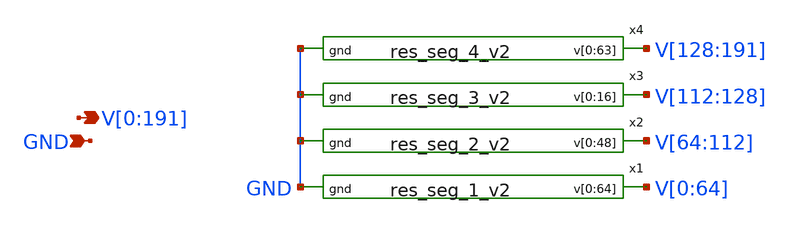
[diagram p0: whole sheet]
** sch_path: xschem/rstring_v2.sch
**.subckt rstring_v2
*+ V[0],V[1],V[2],V[3],V[4],V[5],V[6],V[7],V[8],V[9],V[10],V[11],V[12],V[13],V[14],V[15],V[16],V[17],V[18],V[19],V[20],V[21],V[22],V[23],V[24],V[25],V[26],V[27],V[28],V[29],V[30],V[31],V[32],V[33],V[34],V[35],V[36],V[37],V[38],V[39],V[40],V[41],V[42],V[43],V[44],V[45],V[46],V[47],V[48],V[49],V[50],V[51],V[52],V[53],V[54],V[55],V[56],V[57],V[58],V[59],V[60],V[61],V[62],V[63],V[64],V[65],V[66],V[67],V[68],V[69],V[70],V[71],V[72],V[73],V[74],V[75],V[76],V[77],V[78],V[79],V[80],V[81],V[82],V[83],V[84],V[85],V[86],V[87],V[88],V[89],V[90],V[91],V[92],V[93],V[94],V[95],V[96],V[97],V[98],V[99],V[100],V[101],V[102],V[103],V[104],V[105],V[106],V[107],V[108],V[109],V[110],V[111],V[112],V[113],V[114],V[115],V[116],V[117],V[118],V[119],V[120],V[121],V[122],V[123],V[124],V[125],V[126],V[127],V[128],V[129],V[130],V[131],V[132],V[133],V[134],V[135],V[136],V[137],V[138],V[139],V[140],V[141],V[142],V[143],V[144],V[145],V[146],V[147],V[148],V[149],V[150],V[151],V[152],V[153],V[154],V[155],V[156],V[157],V[158],V[159],V[160],V[161],V[162],V[163],V[164],V[165],V[166],V[167],V[168],V[169],V[170],V[171],V[172],V[173],V[174],V[175],V[176],V[177],V[178],V[179],V[180],V[181],V[182],V[183],V[184],V[185],V[186],V[187],V[188],V[189],V[190],V[191] GND
*.opin
*+ V[0],V[1],V[2],V[3],V[4],V[5],V[6],V[7],V[8],V[9],V[10],V[11],V[12],V[13],V[14],V[15],V[16],V[17],V[18],V[19],V[20],V[21],V[22],V[23],V[24],V[25],V[26],V[27],V[28],V[29],V[30],V[31],V[32],V[33],V[34],V[35],V[36],V[37],V[38],V[39],V[40],V[41],V[42],V[43],V[44],V[45],V[46],V[47],V[48],V[49],V[50],V[51],V[52],V[53],V[54],V[55],V[56],V[57],V[58],V[59],V[60],V[61],V[62],V[63],V[64],V[65],V[66],V[67],V[68],V[69],V[70],V[71],V[72],V[73],V[74],V[75],V[76],V[77],V[78],V[79],V[80],V[81],V[82],V[83],V[84],V[85],V[86],V[87],V[88],V[89],V[90],V[91],V[92],V[93],V[94],V[95],V[96],V[97],V[98],V[99],V[100],V[101],V[102],V[103],V[104],V[105],V[106],V[107],V[108],V[109],V[110],V[111],V[112],V[113],V[114],V[115],V[116],V[117],V[118],V[119],V[120],V[121],V[122],V[123],V[124],V[125],V[126],V[127],V[128],V[129],V[130],V[131],V[132],V[133],V[134],V[135],V[136],V[137],V[138],V[139],V[140],V[141],V[142],V[143],V[144],V[145],V[146],V[147],V[148],V[149],V[150],V[151],V[152],V[153],V[154],V[155],V[156],V[157],V[158],V[159],V[160],V[161],V[162],V[163],V[164],V[165],V[166],V[167],V[168],V[169],V[170],V[171],V[172],V[173],V[174],V[175],V[176],V[177],V[178],V[179],V[180],V[181],V[182],V[183],V[184],V[185],V[186],V[187],V[188],V[189],V[190],V[191]
*.ipin GND
x1 V[0] V[1] V[2] V[3] V[4] V[5] V[6] V[7] V[8] V[9] V[10] V[11] V[12] V[13] V[14] V[15] V[16] V[17]
+ V[18] V[19] V[20] V[21] V[22] V[23] V[24] V[25] V[26] V[27] V[28] V[29] V[30] V[31] V[32] V[33] V[34]
+ V[35] V[36] V[37] V[38] V[39] V[40] V[41] V[42] V[43] V[44] V[45] V[46] V[47] V[48] V[49] V[50] V[51]
+ V[52] V[53] V[54] V[55] V[56] V[57] V[58] V[59] V[60] V[61] V[62] V[63] V[64] GND res_seg_1_v2
x2 V[64] V[65] V[66] V[67] V[68] V[69] V[70] V[71] V[72] V[73] V[74] V[75] V[76] V[77] V[78] V[79]
+ V[80] V[81] V[82] V[83] V[84] V[85] V[86] V[87] V[88] V[89] V[90] V[91] V[92] V[93] V[94] V[95] V[96]
+ V[97] V[98] V[99] V[100] V[101] V[102] V[103] V[104] V[105] V[106] V[107] V[108] V[109] V[110] V[111]
+ V[112] GND res_seg_2_v2
x3 V[112] V[113] V[114] V[115] V[116] V[117] V[118] V[119] V[120] V[121] V[122] V[123] V[124] V[125]
+ V[126] V[127] V[128] GND res_seg_3_v2
x4 V[128] V[129] V[130] V[131] V[132] V[133] V[134] V[135] V[136] V[137] V[138] V[139] V[140] V[141]
+ V[142] V[143] V[144] V[145] V[146] V[147] V[148] V[149] V[150] V[151] V[152] V[153] V[154] V[155] V[156]
+ V[157] V[158] V[159] V[160] V[161] V[162] V[163] V[164] V[165] V[166] V[167] V[168] V[169] V[170] V[171]
+ V[172] V[173] V[174] V[175] V[176] V[177] V[178] V[179] V[180] V[181] V[182] V[183] V[184] V[185] V[186]
+ V[187] V[188] V[189] V[190] V[191] GND res_seg_4_v2
**.ends

* expanding   symbol:  res_seg_1_v2.sym # of pins=2
** sym_path: xschem/res_seg_1_v2.sym
** sch_path: xschem/res_seg_1_v2.sch
.subckt res_seg_1_v2 v[0] v[1] v[2] v[3] v[4] v[5] v[6] v[7] v[8] v[9] v[10] v[11] v[12] v[13] v[14]
+ v[15] v[16] v[17] v[18] v[19] v[20] v[21] v[22] v[23] v[24] v[25] v[26] v[27] v[28] v[29] v[30] v[31]
+ v[32] v[33] v[34] v[35] v[36] v[37] v[38] v[39] v[40] v[41] v[42] v[43] v[44] v[45] v[46] v[47] v[48]
+ v[49] v[50] v[51] v[52] v[53] v[54] v[55] v[56] v[57] v[58] v[59] v[60] v[61] v[62] v[63] v[64] gnd
*.opin
*+ v[0],v[1],v[2],v[3],v[4],v[5],v[6],v[7],v[8],v[9],v[10],v[11],v[12],v[13],v[14],v[15],v[16],v[17],v[18],v[19],v[20],v[21],v[22],v[23],v[24],v[25],v[26],v[27],v[28],v[29],v[30],v[31],v[32],v[33],v[34],v[35],v[36],v[37],v[38],v[39],v[40],v[41],v[42],v[43],v[44],v[45],v[46],v[47],v[48],v[49],v[50],v[51],v[52],v[53],v[54],v[55],v[56],v[57],v[58],v[59],v[60],v[61],v[62],v[63],v[64]
*.ipin gnd
XR1 v[1] V[0] gnd sky130_fd_pr__res_xhigh_po_0p35 L=0.8375 mult=1 m=1
XR2 v[2] v[1] gnd sky130_fd_pr__res_xhigh_po_0p35 L=0.7349 mult=1 m=1
XR3 v[3] v[2] gnd sky130_fd_pr__res_xhigh_po_0p35 L=0.6495 mult=1 m=1
XR4 v[4] v[3] gnd sky130_fd_pr__res_xhigh_po_0p35 L=0.5897 mult=1 m=1
XR8 v[7] v[8] gnd sky130_fd_pr__res_xhigh_po_0p69 L=0.8761 mult=1 m=1
XR9 v[8] v[9] gnd sky130_fd_pr__res_xhigh_po_0p69 L=0.8255 mult=1 m=1
XR10 v[9] v[10] gnd sky130_fd_pr__res_xhigh_po_0p69 L=0.775 mult=1 m=1
XR11 v[10] v[11] gnd sky130_fd_pr__res_xhigh_po_0p69 L=0.7413 mult=1 m=1
XR12 v[11] v[12] gnd sky130_fd_pr__res_xhigh_po_0p69 L=0.7076 mult=1 m=1
XR13 v[12] v[13] gnd sky130_fd_pr__res_xhigh_po_0p69 L=0.6739 mult=1 m=1
XR14 v[13] v[14] gnd sky130_fd_pr__res_xhigh_po_0p69 L=0.657 mult=1 m=1
XR15 v[14] v[15] gnd sky130_fd_pr__res_xhigh_po_0p69 L=0.6234 mult=1 m=1
XR16 v[15] v[16] gnd sky130_fd_pr__res_xhigh_po_0p69 L=0.6065 mult=1 m=1
XR17 v[16] v[17] gnd sky130_fd_pr__res_xhigh_po_0p69 L=0.5728 mult=1 m=1
XR19 v[18] v[19] gnd sky130_fd_pr__res_xhigh_po_0p69 L=0.5391 mult=1 m=1
XR27 v[26] v[27] gnd sky130_fd_pr__res_xhigh_po_1p41 L=0.8951 mult=1 m=1
XR29 v[28] v[29] gnd sky130_fd_pr__res_xhigh_po_1p41 L=0.8607 mult=1 m=1
XR31 v[30] v[31] gnd sky130_fd_pr__res_xhigh_po_1p41 L=0.8263 mult=1 m=1
XR33 v[32] v[33] gnd sky130_fd_pr__res_xhigh_po_1p41 L=0.7918 mult=1 m=1
XR36 v[35] v[36] gnd sky130_fd_pr__res_xhigh_po_1p41 L=0.7574 mult=1 m=1
XR37 v[36] v[37] gnd sky130_fd_pr__res_xhigh_po_1p41 L=0.723 mult=1 m=1
XR40 v[39] v[40] gnd sky130_fd_pr__res_xhigh_po_1p41 L=0.6885 mult=1 m=1
XR41 v[40] v[41] gnd sky130_fd_pr__res_xhigh_po_1p41 L=0.723 mult=1 m=1
XR42 v[41] v[42] gnd sky130_fd_pr__res_xhigh_po_1p41 L=0.6885 mult=1 m=1
XR43 v[42] v[43] gnd sky130_fd_pr__res_xhigh_po_1p41 L=0.6541 mult=1 m=1
XR45 v[44] v[45] gnd sky130_fd_pr__res_xhigh_po_1p41 L=0.6541 mult=1 m=1
XR48 v[47] v[48] gnd sky130_fd_pr__res_xhigh_po_1p41 L=0.6197 mult=1 m=1
XR49 v[48] v[49] gnd sky130_fd_pr__res_xhigh_po_1p41 L=0.6541 mult=1 m=1
XR51 v[50] v[51] gnd sky130_fd_pr__res_xhigh_po_1p41 L=0.5853 mult=1 m=1
XR52 v[51] v[52] gnd sky130_fd_pr__res_xhigh_po_1p41 L=0.6197 mult=1 m=1
XR53 v[52] v[53] gnd sky130_fd_pr__res_xhigh_po_1p41 L=0.5853 mult=1 m=1
XR58 v[57] v[58] gnd sky130_fd_pr__res_xhigh_po_1p41 L=0.5508 mult=1 m=1
XR64 v[63] v[64] gnd sky130_fd_pr__res_xhigh_po_1p41 L=0.5164 mult=1 m=1
XR5 v[5] v[4] gnd sky130_fd_pr__res_xhigh_po_0p35 L=0.5469 mult=1 m=1
XR6 v[6] v[5] gnd sky130_fd_pr__res_xhigh_po_0p35 L=0.5042 mult=1 m=1
XR21 v[20] v[21] gnd sky130_fd_pr__res_xhigh_po_0p69 L=0.5054 mult=1 m=1
XR54 v[53] v[54] gnd sky130_fd_pr__res_xhigh_po_1p41 L=0.5853 mult=1 m=1
XR7 v[6] v[7] gnd sky130_fd_pr__res_xhigh_po_0p69 L=0.9266 mult=1 m=1
XR18 v[17] v[18] gnd sky130_fd_pr__res_xhigh_po_0p69 L=0.5728 mult=1 m=1
XR20 v[19] v[20] gnd sky130_fd_pr__res_xhigh_po_0p69 L=0.5391 mult=1 m=1
XR22 v[21] v[22] gnd sky130_fd_pr__res_xhigh_po_0p69 L=0.5054 mult=1 m=1
XR23 v[22] v[23] gnd sky130_fd_pr__res_xhigh_po_1p41 L=0.9984 mult=1 m=1
XR24 v[23] v[24] gnd sky130_fd_pr__res_xhigh_po_1p41 L=0.9984 mult=1 m=1
XR25 v[24] v[25] gnd sky130_fd_pr__res_xhigh_po_1p41 L=0.9295 mult=1 m=1
XR26 v[25] v[26] gnd sky130_fd_pr__res_xhigh_po_1p41 L=0.9295 mult=1 m=1
XR28 v[27] v[28] gnd sky130_fd_pr__res_xhigh_po_1p41 L=0.8951 mult=1 m=1
XR30 v[29] v[30] gnd sky130_fd_pr__res_xhigh_po_1p41 L=0.8607 mult=1 m=1
XR32 v[31] v[32] gnd sky130_fd_pr__res_xhigh_po_1p41 L=0.8263 mult=1 m=1
XR34 v[33] v[34] gnd sky130_fd_pr__res_xhigh_po_1p41 L=0.7918 mult=1 m=1
XR35 v[34] v[35] gnd sky130_fd_pr__res_xhigh_po_1p41 L=0.7918 mult=1 m=1
XR38 v[37] v[38] gnd sky130_fd_pr__res_xhigh_po_1p41 L=0.7574 mult=1 m=1
XR39 v[38] v[39] gnd sky130_fd_pr__res_xhigh_po_1p41 L=0.723 mult=1 m=1
XR44 v[43] v[44] gnd sky130_fd_pr__res_xhigh_po_1p41 L=0.6885 mult=1 m=1
XR46 v[45] v[46] gnd sky130_fd_pr__res_xhigh_po_1p41 L=0.6541 mult=1 m=1
XR47 v[46] v[47] gnd sky130_fd_pr__res_xhigh_po_1p41 L=0.6541 mult=1 m=1
XR50 v[49] v[50] gnd sky130_fd_pr__res_xhigh_po_1p41 L=0.6197 mult=1 m=1
XR55 v[54] v[55] gnd sky130_fd_pr__res_xhigh_po_1p41 L=0.5853 mult=1 m=1
XR56 v[55] v[56] gnd sky130_fd_pr__res_xhigh_po_1p41 L=0.5853 mult=1 m=1
XR57 v[56] v[57] gnd sky130_fd_pr__res_xhigh_po_1p41 L=0.5853 mult=1 m=1
XR59 v[58] v[59] gnd sky130_fd_pr__res_xhigh_po_1p41 L=0.5508 mult=1 m=1
XR60 v[59] v[60] gnd sky130_fd_pr__res_xhigh_po_1p41 L=0.5508 mult=1 m=1
XR61 v[60] v[61] gnd sky130_fd_pr__res_xhigh_po_1p41 L=0.5508 mult=1 m=1
XR62 v[61] v[62] gnd sky130_fd_pr__res_xhigh_po_1p41 L=0.5508 mult=1 m=1
XR63 v[62] v[63] gnd sky130_fd_pr__res_xhigh_po_1p41 L=0.5508 mult=1 m=1
.ends


* expanding   symbol:  res_seg_2_v2.sym # of pins=2
** sym_path: xschem/res_seg_2_v2.sym
** sch_path: xschem/res_seg_2_v2.sch
.subckt res_seg_2_v2 v[0] v[1] v[2] v[3] v[4] v[5] v[6] v[7] v[8] v[9] v[10] v[11] v[12] v[13] v[14]
+ v[15] v[16] v[17] v[18] v[19] v[20] v[21] v[22] v[23] v[24] v[25] v[26] v[27] v[28] v[29] v[30] v[31]
+ v[32] v[33] v[34] v[35] v[36] v[37] v[38] v[39] v[40] v[41] v[42] v[43] v[44] v[45] v[46] v[47] v[48] gnd
*.opin
*+ v[0],v[1],v[2],v[3],v[4],v[5],v[6],v[7],v[8],v[9],v[10],v[11],v[12],v[13],v[14],v[15],v[16],v[17],v[18],v[19],v[20],v[21],v[22],v[23],v[24],v[25],v[26],v[27],v[28],v[29],v[30],v[31],v[32],v[33],v[34],v[35],v[36],v[37],v[38],v[39],v[40],v[41],v[42],v[43],v[44],v[45],v[46],v[47],v[48]
*.ipin gnd
XR1 v[1] v[0] gnd sky130_fd_pr__res_xhigh_po_0p35 L=1.9570 mult=1 m=1
XR2 v[2] v[1] gnd sky130_fd_pr__res_xhigh_po_0p35 L=1.7348 mult=1 m=1
XR3 v[3] v[2] gnd sky130_fd_pr__res_xhigh_po_0p35 L=1.5639 mult=1 m=1
XR4 v[4] v[3] gnd sky130_fd_pr__res_xhigh_po_0p35 L=1.4442 mult=1 m=1
XR5 v[5] v[4] gnd sky130_fd_pr__res_xhigh_po_0p35 L=1.3417 mult=1 m=1
XR6 v[6] v[5] gnd sky130_fd_pr__res_xhigh_po_0p35 L=1.2648 mult=1 m=1
XR7 v[7] v[6] gnd sky130_fd_pr__res_xhigh_po_0p35 L=1.1964 mult=1 m=1
XR8 v[8] v[7] gnd sky130_fd_pr__res_xhigh_po_0p35 L=1.1366 mult=1 m=1
XR9 v[9] v[8] gnd sky130_fd_pr__res_xhigh_po_0p35 L=1.0853 mult=1 m=1
XR10 v[10] v[9] gnd sky130_fd_pr__res_xhigh_po_0p35 L=1.0511 mult=1 m=1
XR11 v[11] v[10] gnd sky130_fd_pr__res_xhigh_po_0p35 L=1.0169 mult=1 m=1
XR12 v[12] v[11] gnd sky130_fd_pr__res_xhigh_po_0p35 L=0.9828 mult=1 m=1
XR13 v[13] v[12] gnd sky130_fd_pr__res_xhigh_po_0p35 L=0.9571 mult=1 m=1
XR14 v[14] v[13] gnd sky130_fd_pr__res_xhigh_po_0p35 L=0.94 mult=1 m=1
XR15 v[15] v[14] gnd sky130_fd_pr__res_xhigh_po_0p35 L=0.9144 mult=1 m=1
XR16 v[16] v[15] gnd sky130_fd_pr__res_xhigh_po_0p35 L=0.8888 mult=1 m=1
XR17 v[17] v[16] gnd sky130_fd_pr__res_xhigh_po_0p35 L=0.8802 mult=1 m=1
XR18 v[18] v[17] gnd sky130_fd_pr__res_xhigh_po_0p35 L=0.8717 mult=1 m=1
XR19 v[19] v[18] gnd sky130_fd_pr__res_xhigh_po_0p35 L=0.8546 mult=1 m=1
XR20 v[20] v[19] gnd sky130_fd_pr__res_xhigh_po_0p35 L=0.8375 mult=1 m=1
XR22 v[22] v[21] gnd sky130_fd_pr__res_xhigh_po_0p35 L=0.8289 mult=1 m=1
XR23 v[23] v[22] gnd sky130_fd_pr__res_xhigh_po_0p35 L=0.8204 mult=1 m=1
XR24 v[24] v[23] gnd sky130_fd_pr__res_xhigh_po_0p35 L=0.8118 mult=1 m=1
XR33 v[33] v[32] gnd sky130_fd_pr__res_xhigh_po_0p35 L=0.8204 mult=1 m=1
XR35 v[35] v[34] gnd sky130_fd_pr__res_xhigh_po_0p35 L=0.8289 mult=1 m=1
XR36 v[36] v[35] gnd sky130_fd_pr__res_xhigh_po_0p35 L=0.8375 mult=1 m=1
XR38 v[38] v[37] gnd sky130_fd_pr__res_xhigh_po_0p35 L=0.8631 mult=1 m=1
XR40 v[40] v[39] gnd sky130_fd_pr__res_xhigh_po_0p35 L=0.8888 mult=1 m=1
XR41 v[41] v[40] gnd sky130_fd_pr__res_xhigh_po_0p35 L=0.8973 mult=1 m=1
XR42 v[42] v[41] gnd sky130_fd_pr__res_xhigh_po_0p35 L=0.9144 mult=1 m=1
XR43 v[43] v[42] gnd sky130_fd_pr__res_xhigh_po_0p35 L=0.94 mult=1 m=1
XR44 v[44] v[43] gnd sky130_fd_pr__res_xhigh_po_0p35 L=0.9571 mult=1 m=1
XR45 v[45] v[44] gnd sky130_fd_pr__res_xhigh_po_0p35 L=0.9828 mult=1 m=1
XR46 v[46] v[45] gnd sky130_fd_pr__res_xhigh_po_0p35 L=1.0084 mult=1 m=1
XR47 v[47] v[46] gnd sky130_fd_pr__res_xhigh_po_0p35 L=1.0426 mult=1 m=1
XR48 v[48] v[47] gnd sky130_fd_pr__res_xhigh_po_0p35 L=1.0853 mult=1 m=1
XR37 v[37] v[36] gnd sky130_fd_pr__res_xhigh_po_0p35 L=0.846 mult=1 m=1
XR21 v[21] v[20] gnd sky130_fd_pr__res_xhigh_po_0p35 L=0.8375 mult=1 m=1
XR25 v[25] v[24] gnd sky130_fd_pr__res_xhigh_po_0p35 L=0.8118 mult=1 m=1
XR26 v[26] v[25] gnd sky130_fd_pr__res_xhigh_po_0p35 L=0.8118 mult=1 m=1
XR27 v[27] v[26] gnd sky130_fd_pr__res_xhigh_po_0p35 L=0.8033 mult=1 m=1
XR28 v[28] v[27] gnd sky130_fd_pr__res_xhigh_po_0p35 L=0.8118 mult=1 m=1
XR29 v[29] v[28] gnd sky130_fd_pr__res_xhigh_po_0p35 L=0.8033 mult=1 m=1
XR30 v[30] v[29] gnd sky130_fd_pr__res_xhigh_po_0p35 L=0.8033 mult=1 m=1
XR31 v[31] v[30] gnd sky130_fd_pr__res_xhigh_po_0p35 L=0.8118 mult=1 m=1
XR32 v[32] v[31] gnd sky130_fd_pr__res_xhigh_po_0p35 L=0.8118 mult=1 m=1
XR34 v[34] v[33] gnd sky130_fd_pr__res_xhigh_po_0p35 L=0.8204 mult=1 m=1
XR39 v[39] v[38] gnd sky130_fd_pr__res_xhigh_po_0p35 L=0.8631 mult=1 m=1
.ends


* expanding   symbol:  res_seg_3_v2.sym # of pins=2
** sym_path: xschem/res_seg_3_v2.sym
** sch_path: xschem/res_seg_3_v2.sch
.subckt res_seg_3_v2 v[0] v[1] v[2] v[3] v[4] v[5] v[6] v[7] v[8] v[9] v[10] v[11] v[12] v[13] v[14]
+ v[15] v[16] gnd
*.opin v[0],v[1],v[2],v[3],v[4],v[5],v[6],v[7],v[8],v[9],v[10],v[11],v[12],v[13],v[14],v[15],v[16]
*.ipin gnd
XR1 v[0] v[1] gnd sky130_fd_pr__res_xhigh_po_0p35 L=0.5555 mult=1 m=1
XR2 v[1] v[2] gnd sky130_fd_pr__res_xhigh_po_0p35 L=0.5726 mult=1 m=1
XR3 v[2] v[3] gnd sky130_fd_pr__res_xhigh_po_0p35 L=0.5811 mult=1 m=1
XR4 v[3] v[4] gnd sky130_fd_pr__res_xhigh_po_0p35 L=0.5897 mult=1 m=1
XR5 v[4] v[5] gnd sky130_fd_pr__res_xhigh_po_0p35 L=0.6153 mult=1 m=1
XR6 v[5] v[6] gnd sky130_fd_pr__res_xhigh_po_0p35 L=0.6238 mult=1 m=1
XR7 v[6] v[7] gnd sky130_fd_pr__res_xhigh_po_0p35 L=0.6409 mult=1 m=1
XR8 v[7] v[8] gnd sky130_fd_pr__res_xhigh_po_0p35 L=0.6666 mult=1 m=1
XR9 v[8] v[9] gnd sky130_fd_pr__res_xhigh_po_0p35 L=0.6837 mult=1 m=1
XR10 v[9] v[10] gnd sky130_fd_pr__res_xhigh_po_0p35 L=0.7093 mult=1 m=1
XR11 v[10] v[11] gnd sky130_fd_pr__res_xhigh_po_0p35 L=0.7264 mult=1 m=1
XR12 v[11] v[12] gnd sky130_fd_pr__res_xhigh_po_0p35 L=0.7691 mult=1 m=1
XR13 v[12] v[13] gnd sky130_fd_pr__res_xhigh_po_0p35 L=0.7948 mult=1 m=1
XR14 v[13] v[14] gnd sky130_fd_pr__res_xhigh_po_0p35 L=0.8375 mult=1 m=1
XR15 v[14] v[15] gnd sky130_fd_pr__res_xhigh_po_0p35 L=0.8802 mult=1 m=1
XR16 v[15] v[16] gnd sky130_fd_pr__res_xhigh_po_0p35 L=0.9315 mult=1 m=1
.ends


* expanding   symbol:  res_seg_4_v2.sym # of pins=2
** sym_path: xschem/res_seg_4_v2.sym
** sch_path: xschem/res_seg_4_v2.sch
.subckt res_seg_4_v2 v[0] v[1] v[2] v[3] v[4] v[5] v[6] v[7] v[8] v[9] v[10] v[11] v[12] v[13] v[14]
+ v[15] v[16] v[17] v[18] v[19] v[20] v[21] v[22] v[23] v[24] v[25] v[26] v[27] v[28] v[29] v[30] v[31]
+ v[32] v[33] v[34] v[35] v[36] v[37] v[38] v[39] v[40] v[41] v[42] v[43] v[44] v[45] v[46] v[47] v[48]
+ v[49] v[50] v[51] v[52] v[53] v[54] v[55] v[56] v[57] v[58] v[59] v[60] v[61] v[62] v[63] gnd
*.opin
*+ v[0],v[1],v[2],v[3],v[4],v[5],v[6],v[7],v[8],v[9],v[10],v[11],v[12],v[13],v[14],v[15],v[16],v[17],v[18],v[19],v[20],v[21],v[22],v[23],v[24],v[25],v[26],v[27],v[28],v[29],v[30],v[31],v[32],v[33],v[34],v[35],v[36],v[37],v[38],v[39],v[40],v[41],v[42],v[43],v[44],v[45],v[46],v[47],v[48],v[49],v[50],v[51],v[52],v[53],v[54],v[55],v[56],v[57],v[58],v[59],v[60],v[61],v[62],v[63]
*.ipin gnd
XR7 v[6] v[7] gnd sky130_fd_pr__res_xhigh_po_1p41 L=0.5164 mult=1 m=1
XR10 v[9] v[10] gnd sky130_fd_pr__res_xhigh_po_1p41 L=0.5508 mult=1 m=1
XR17 v[16] v[17] gnd sky130_fd_pr__res_xhigh_po_1p41 L=0.5853 mult=1 m=1
XR28 v[27] v[28] gnd sky130_fd_pr__res_xhigh_po_1p41 L=0.6541 mult=1 m=1
XR31 v[30] v[31] gnd sky130_fd_pr__res_xhigh_po_1p41 L=0.6885 mult=1 m=1
XR36 v[35] v[36] gnd sky130_fd_pr__res_xhigh_po_1p41 L=0.7574 mult=1 m=1
XR37 v[36] v[37] gnd sky130_fd_pr__res_xhigh_po_1p41 L=0.723 mult=1 m=1
XR40 v[39] v[40] gnd sky130_fd_pr__res_xhigh_po_1p41 L=0.7918 mult=1 m=1
XR43 v[42] v[43] gnd sky130_fd_pr__res_xhigh_po_1p41 L=0.8263 mult=1 m=1
XR44 v[43] v[44] gnd sky130_fd_pr__res_xhigh_po_1p41 L=0.8607 mult=1 m=1
XR46 v[45] v[46] gnd sky130_fd_pr__res_xhigh_po_1p41 L=0.8951 mult=1 m=1
XR51 v[50] v[51] gnd sky130_fd_pr__res_xhigh_po_0p69 L=0.5054 mult=1 m=1
XR53 v[52] v[53] gnd sky130_fd_pr__res_xhigh_po_0p69 L=0.5391 mult=1 m=1
XR55 v[54] v[55] gnd sky130_fd_pr__res_xhigh_po_0p69 L=0.5728 mult=1 m=1
XR56 v[55] v[56] gnd sky130_fd_pr__res_xhigh_po_0p69 L=0.5897 mult=1 m=1
XR57 v[56] v[57] gnd sky130_fd_pr__res_xhigh_po_0p69 L=0.6234 mult=1 m=1
XR58 v[57] v[58] gnd sky130_fd_pr__res_xhigh_po_0p69 L=0.6402 mult=1 m=1
XR59 v[58] v[59] gnd sky130_fd_pr__res_xhigh_po_0p69 L=0.6907 mult=1 m=1
XR60 v[59] v[60] gnd sky130_fd_pr__res_xhigh_po_0p69 L=0.7244 mult=1 m=1
XR61 v[60] v[61] gnd sky130_fd_pr__res_xhigh_po_0p69 L=0.7581 mult=1 m=1
XR8 v[7] v[8] gnd sky130_fd_pr__res_xhigh_po_1p41 L=0.5164 mult=1 m=1
XR11 v[10] v[11] gnd sky130_fd_pr__res_xhigh_po_1p41 L=0.5164 mult=1 m=1
XR12 v[11] v[12] gnd sky130_fd_pr__res_xhigh_po_1p41 L=0.5508 mult=1 m=1
XR13 v[12] v[13] gnd sky130_fd_pr__res_xhigh_po_1p41 L=0.5164 mult=1 m=1
XR23 v[22] v[23] gnd sky130_fd_pr__res_xhigh_po_1p41 L=0.6197 mult=1 m=1
XR34 v[33] v[34] gnd sky130_fd_pr__res_xhigh_po_1p41 L=0.723 mult=1 m=1
XR41 v[40] v[41] gnd sky130_fd_pr__res_xhigh_po_1p41 L=0.7918 mult=1 m=1
XR1 v[0] v[1] gnd sky130_fd_pr__res_xhigh_po_2p85 L=0.9742 mult=1 m=1
XR2 v[1] v[2] gnd sky130_fd_pr__res_xhigh_po_2p85 L=0.9742 mult=1 m=1
XR4 v[3] v[4] gnd sky130_fd_pr__res_xhigh_po_2p85 L=0.9742 mult=1 m=1
XR6 v[5] v[6] gnd sky130_fd_pr__res_xhigh_po_2p85 L=0.9742 mult=1 m=1
XR3 v[2] v[3] gnd sky130_fd_pr__res_xhigh_po_2p85 L=1.0438 mult=1 m=1
XR5 v[4] v[5] gnd sky130_fd_pr__res_xhigh_po_2p85 L=1.0438 mult=1 m=1
XR9 v[8] v[9] gnd sky130_fd_pr__res_xhigh_po_1p41 L=0.5164 mult=1 m=1
XR14 v[13] v[14] gnd sky130_fd_pr__res_xhigh_po_1p41 L=0.5508 mult=1 m=1
XR15 v[14] v[15] gnd sky130_fd_pr__res_xhigh_po_1p41 L=0.5508 mult=1 m=1
XR16 v[15] v[16] gnd sky130_fd_pr__res_xhigh_po_1p41 L=0.5508 mult=1 m=1
XR18 v[17] v[18] gnd sky130_fd_pr__res_xhigh_po_1p41 L=0.5508 mult=1 m=1
XR19 v[18] v[19] gnd sky130_fd_pr__res_xhigh_po_1p41 L=0.5853 mult=1 m=1
XR20 v[19] v[20] gnd sky130_fd_pr__res_xhigh_po_1p41 L=0.5853 mult=1 m=1
XR21 v[20] v[21] gnd sky130_fd_pr__res_xhigh_po_1p41 L=0.5853 mult=1 m=1
XR22 v[21] v[22] gnd sky130_fd_pr__res_xhigh_po_1p41 L=0.5853 mult=1 m=1
XR24 v[23] v[24] gnd sky130_fd_pr__res_xhigh_po_1p41 L=0.6197 mult=1 m=1
XR25 v[24] v[25] gnd sky130_fd_pr__res_xhigh_po_1p41 L=0.6197 mult=1 m=1
XR26 v[25] v[26] gnd sky130_fd_pr__res_xhigh_po_1p41 L=0.6197 mult=1 m=1
XR27 v[26] v[27] gnd sky130_fd_pr__res_xhigh_po_1p41 L=0.6197 mult=1 m=1
XR29 v[28] v[29] gnd sky130_fd_pr__res_xhigh_po_1p41 L=0.6541 mult=1 m=1
XR30 v[29] v[30] gnd sky130_fd_pr__res_xhigh_po_1p41 L=0.6541 mult=1 m=1
XR32 v[31] v[32] gnd sky130_fd_pr__res_xhigh_po_1p41 L=0.6541 mult=1 m=1
XR33 v[32] v[33] gnd sky130_fd_pr__res_xhigh_po_1p41 L=0.6885 mult=1 m=1
XR35 v[34] v[35] gnd sky130_fd_pr__res_xhigh_po_1p41 L=0.6885 mult=1 m=1
XR38 v[37] v[38] gnd sky130_fd_pr__res_xhigh_po_1p41 L=0.7574 mult=1 m=1
XR39 v[38] v[39] gnd sky130_fd_pr__res_xhigh_po_1p41 L=0.7574 mult=1 m=1
XR42 v[41] v[42] gnd sky130_fd_pr__res_xhigh_po_1p41 L=0.7918 mult=1 m=1
XR45 v[44] v[45] gnd sky130_fd_pr__res_xhigh_po_1p41 L=0.8607 mult=1 m=1
XR47 v[46] v[47] gnd sky130_fd_pr__res_xhigh_po_1p41 L=0.8951 mult=1 m=1
XR48 v[47] v[48] gnd sky130_fd_pr__res_xhigh_po_1p41 L=0.9295 mult=1 m=1
XR49 v[48] v[49] gnd sky130_fd_pr__res_xhigh_po_1p41 L=0.964 mult=1 m=1
XR50 v[49] v[50] gnd sky130_fd_pr__res_xhigh_po_1p41 L=0.964 mult=1 m=1
XR52 v[51] v[52] gnd sky130_fd_pr__res_xhigh_po_0p69 L=0.5054 mult=1 m=1
XR54 v[53] v[54] gnd sky130_fd_pr__res_xhigh_po_0p69 L=0.5391 mult=1 m=1
XR62 v[61] v[62] gnd sky130_fd_pr__res_xhigh_po_0p69 L=0.8424 mult=1 m=1
XR63 v[62] V[63] gnd sky130_fd_pr__res_xhigh_po_0p69 L=0.8929 mult=1 m=1
.ends

.end
